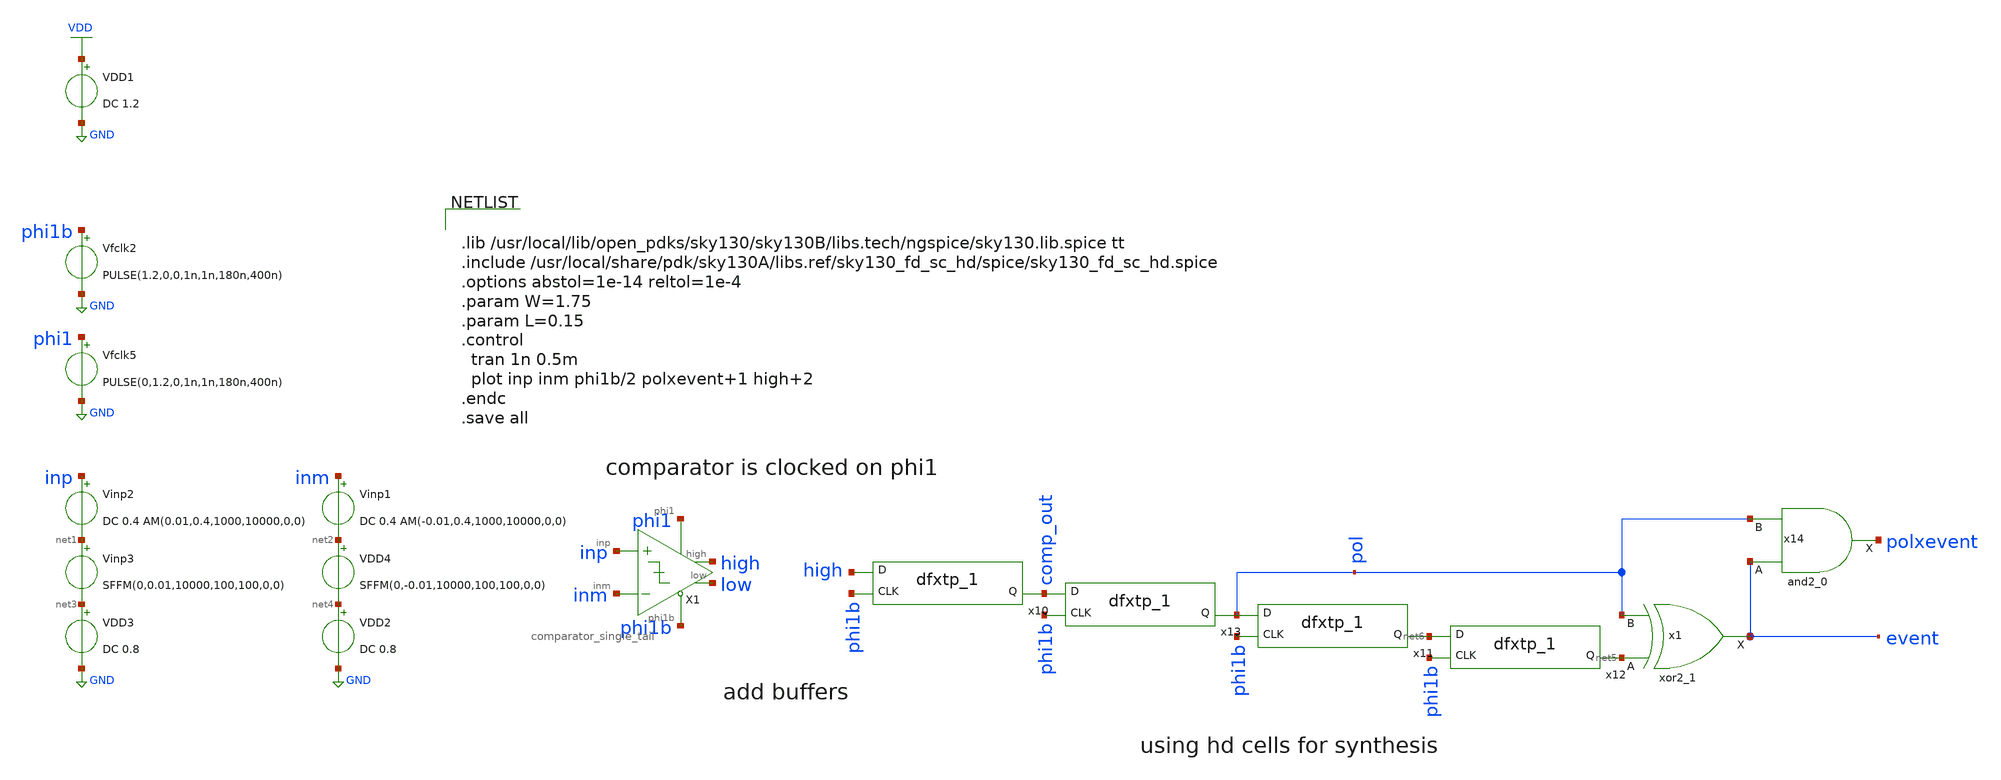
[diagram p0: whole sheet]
** sch_path: xschem/test_bench/comparator_threshold_pol_event_tb.sch
**.subckt comparator_threshold_pol_event_tb
VDD1 VDD GND DC 1.2
Vfclk5 phi1 GND PULSE(0,1.2,0,1n,1n,180n,400n)
Vfclk2 phi1b GND PULSE(1.2,0,0,1n,1n,180n,400n)
Vinp2 inp net1 DC 0.4 AM(0.01,0.4,1000,10000,0,0)
Vinp1 inm net2 DC 0.4 AM(-0.01,0.4,1000,10000,0,0)
Vinp3 net1 net3 SFFM(0,0.01,10000,100,100,0,0)
VDD4 net2 net4 SFFM(0,-0.01,10000,100,100,0,0)
VDD2 net4 GND DC 0.8
VDD3 net3 GND DC 0.8
x1 net5 pol GND GND VDD VDD event sky130_fd_sc_hd__xor2_1
x11 phi1b pol gnd gnd vdd vdd net6 sky130_fd_sc_hd__dfxtp_1
x12 phi1b net6 gnd gnd vdd vdd net5 sky130_fd_sc_hd__dfxtp_1
x10 phi1b high gnd gnd vdd vdd comp_out sky130_fd_sc_hd__dfxtp_1
x13 phi1b comp_out gnd gnd vdd vdd pol sky130_fd_sc_hd__dfxtp_1
x14 event pol GND GND VDD VDD polxevent sky130_fd_sc_hd__and2_0
X1 inp inm high phi1 phi1b low comparator_single_tail Wplus=0.42 Lplus=0.42 Wminus=0.42 Lminus=0.15
**** begin user architecture code


.lib /usr/local/lib/open_pdks/sky130/sky130B/libs.tech/ngspice/sky130.lib.spice tt
.include /usr/local/share/pdk/sky130A/libs.ref/sky130_fd_sc_hd/spice/sky130_fd_sc_hd.spice
.options abstol=1e-14 reltol=1e-4
.param W=1.75
.param L=0.15
.control
  tran 1n 0.5m
  plot inp inm phi1b/2 polxevent+1 high+2
.endc
.save all


**** end user architecture code
**.ends

* expanding   symbol:  comparator_latest/comparator_single_tail.sym # of pins=6
** sym_path: xschem/tryandtest/comparator_single_tail.sym
** sch_path: xschem/tryandtest/comparator_single_tail.sch
.subckt comparator_single_tail inp inm high phi1 phi1b low  Wplus=0.42 Lplus=0.15 Wminus=0.42
+ Lminus=0.15
*.ipin phi1
*.opin high
*.ipin phi1b
*.ipin inp
*.ipin inm
*.opin low
XM1 pfete high VDD VDD sky130_fd_pr__pfet_01v8 L=0.15 W=0.42 nf=1 ad='int((nf+1)/2) * W/nf * 0.29' as='int((nf+2)/2) * W/nf * 0.29'
+ pd='2*int((nf+1)/2) * (W/nf + 0.29)' ps='2*int((nf+2)/2) * (W/nf + 0.29)' nrd='0.29 / W' nrs='0.29 / W'
+ sa=0 sb=0 sd=0 mult=1 m=1
XM2 VDD low pfetw VDD sky130_fd_pr__pfet_01v8 L=0.15 W=0.42 nf=1 ad='int((nf+1)/2) * W/nf * 0.29' as='int((nf+2)/2) * W/nf * 0.29'
+ pd='2*int((nf+1)/2) * (W/nf + 0.29)' ps='2*int((nf+2)/2) * (W/nf + 0.29)' nrd='0.29 / W' nrs='0.29 / W'
+ sa=0 sb=0 sd=0 mult=1 m=1
XM16 pfetw FP high VDD sky130_fd_pr__pfet_01v8 L=0.15 W=0.42 nf=1 ad='int((nf+1)/2) * W/nf * 0.29' as='int((nf+2)/2) * W/nf * 0.29'
+ pd='2*int((nf+1)/2) * (W/nf + 0.29)' ps='2*int((nf+2)/2) * (W/nf + 0.29)' nrd='0.29 / W' nrs='0.29 / W'
+ sa=0 sb=0 sd=0 mult=1 m=1
XM17 low FN pfete VDD sky130_fd_pr__pfet_01v8 L=0.15 W=0.42 nf=1 ad='int((nf+1)/2) * W/nf * 0.29' as='int((nf+2)/2) * W/nf * 0.29'
+ pd='2*int((nf+1)/2) * (W/nf + 0.29)' ps='2*int((nf+2)/2) * (W/nf + 0.29)' nrd='0.29 / W' nrs='0.29 / W'
+ sa=0 sb=0 sd=0 mult=1 m=1
XM3 FN phi1 VDD VDD sky130_fd_pr__pfet_01v8 L=0.15 W=0.42 nf=1 ad='int((nf+1)/2) * W/nf * 0.29' as='int((nf+2)/2) * W/nf * 0.29'
+ pd='2*int((nf+1)/2) * (W/nf + 0.29)' ps='2*int((nf+2)/2) * (W/nf + 0.29)' nrd='0.29 / W' nrs='0.29 / W'
+ sa=0 sb=0 sd=0 mult=1 m=1
XM5 VDD phi1 FP VDD sky130_fd_pr__pfet_01v8 L=0.15 W=0.42 nf=1 ad='int((nf+1)/2) * W/nf * 0.29' as='int((nf+2)/2) * W/nf * 0.29'
+ pd='2*int((nf+1)/2) * (W/nf + 0.29)' ps='2*int((nf+2)/2) * (W/nf + 0.29)' nrd='0.29 / W' nrs='0.29 / W'
+ sa=0 sb=0 sd=0 mult=1 m=1
XM4 high phi1b GND GND sky130_fd_pr__nfet_01v8_lvt L=0.15 W=0.42 nf=1 ad='int((nf+1)/2) * W/nf * 0.29'
+ as='int((nf+2)/2) * W/nf * 0.29' pd='2*int((nf+1)/2) * (W/nf + 0.29)' ps='2*int((nf+2)/2) * (W/nf + 0.29)'
+ nrd='0.29 / W' nrs='0.29 / W' sa=0 sb=0 sd=0 mult=1 m=1
XM7 low high GND GND sky130_fd_pr__nfet_01v8_lvt L=0.15 W=0.42 nf=1 ad='int((nf+1)/2) * W/nf * 0.29'
+ as='int((nf+2)/2) * W/nf * 0.29' pd='2*int((nf+1)/2) * (W/nf + 0.29)' ps='2*int((nf+2)/2) * (W/nf + 0.29)'
+ nrd='0.29 / W' nrs='0.29 / W' sa=0 sb=0 sd=0 mult=1 m=1
XM8 tail inp FP GND sky130_fd_pr__nfet_01v8_lvt L=Lplus W=Wplus nf=1 ad='int((nf+1)/2) * W/nf * 0.29'
+ as='int((nf+2)/2) * W/nf * 0.29' pd='2*int((nf+1)/2) * (W/nf + 0.29)' ps='2*int((nf+2)/2) * (W/nf + 0.29)'
+ nrd='0.29 / W' nrs='0.29 / W' sa=0 sb=0 sd=0 mult=1 m=1
XM6 FN inm tail GND sky130_fd_pr__nfet_01v8_lvt L=Lminus W=Wminus nf=1 ad='int((nf+1)/2) * W/nf * 0.29'
+ as='int((nf+2)/2) * W/nf * 0.29' pd='2*int((nf+1)/2) * (W/nf + 0.29)' ps='2*int((nf+2)/2) * (W/nf + 0.29)'
+ nrd='0.29 / W' nrs='0.29 / W' sa=0 sb=0 sd=0 mult=1 m=1
XM9 GND phi1b low GND sky130_fd_pr__nfet_01v8_lvt L=0.15 W=0.42 nf=1 ad='int((nf+1)/2) * W/nf * 0.29'
+ as='int((nf+2)/2) * W/nf * 0.29' pd='2*int((nf+1)/2) * (W/nf + 0.29)' ps='2*int((nf+2)/2) * (W/nf + 0.29)'
+ nrd='0.29 / W' nrs='0.29 / W' sa=0 sb=0 sd=0 mult=1 m=1
XM10 GND low high GND sky130_fd_pr__nfet_01v8_lvt L=0.15 W=0.42 nf=1 ad='int((nf+1)/2) * W/nf * 0.29'
+ as='int((nf+2)/2) * W/nf * 0.29' pd='2*int((nf+1)/2) * (W/nf + 0.29)' ps='2*int((nf+2)/2) * (W/nf + 0.29)'
+ nrd='0.29 / W' nrs='0.29 / W' sa=0 sb=0 sd=0 mult=1 m=1
XM11 GND phi1 tail GND sky130_fd_pr__nfet_01v8_lvt L=0.15 W=0.42 nf=1 ad='int((nf+1)/2) * W/nf * 0.29'
+ as='int((nf+2)/2) * W/nf * 0.29' pd='2*int((nf+1)/2) * (W/nf + 0.29)' ps='2*int((nf+2)/2) * (W/nf + 0.29)'
+ nrd='0.29 / W' nrs='0.29 / W' sa=0 sb=0 sd=0 mult=1 m=1
.ends

.GLOBAL GND
.GLOBAL VDD
.end
